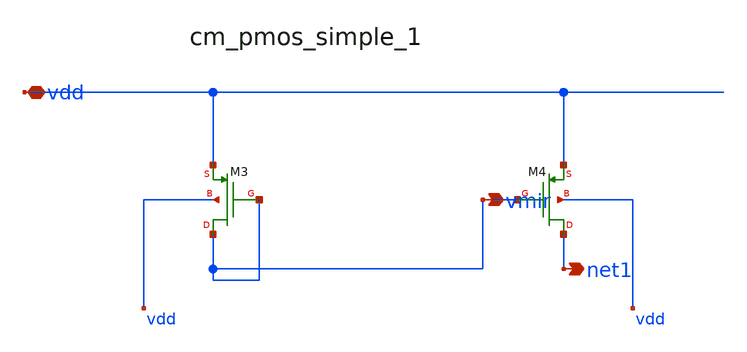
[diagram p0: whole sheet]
** sch_path: analog-db/raw/tsn_002_ptat_classic/hier/blocks/cm_pmos_simple_1.sch
**.subckt cm_pmos_simple_1 vdd vmir net1
*.iopin vdd
*.opin vmir
*.opin net1
XM3 vmir vmir vdd vdd sg13_lv_pmos w=x_dut_xm3_w l=x_dut_xm3_l ng=1 m=x_dut_xm3_m
XM4 net1 vmir vdd vdd sg13_lv_pmos w=x_dut_xm4_w l=x_dut_xm4_l ng=1 m=x_dut_xm4_m
**.ends
.end
